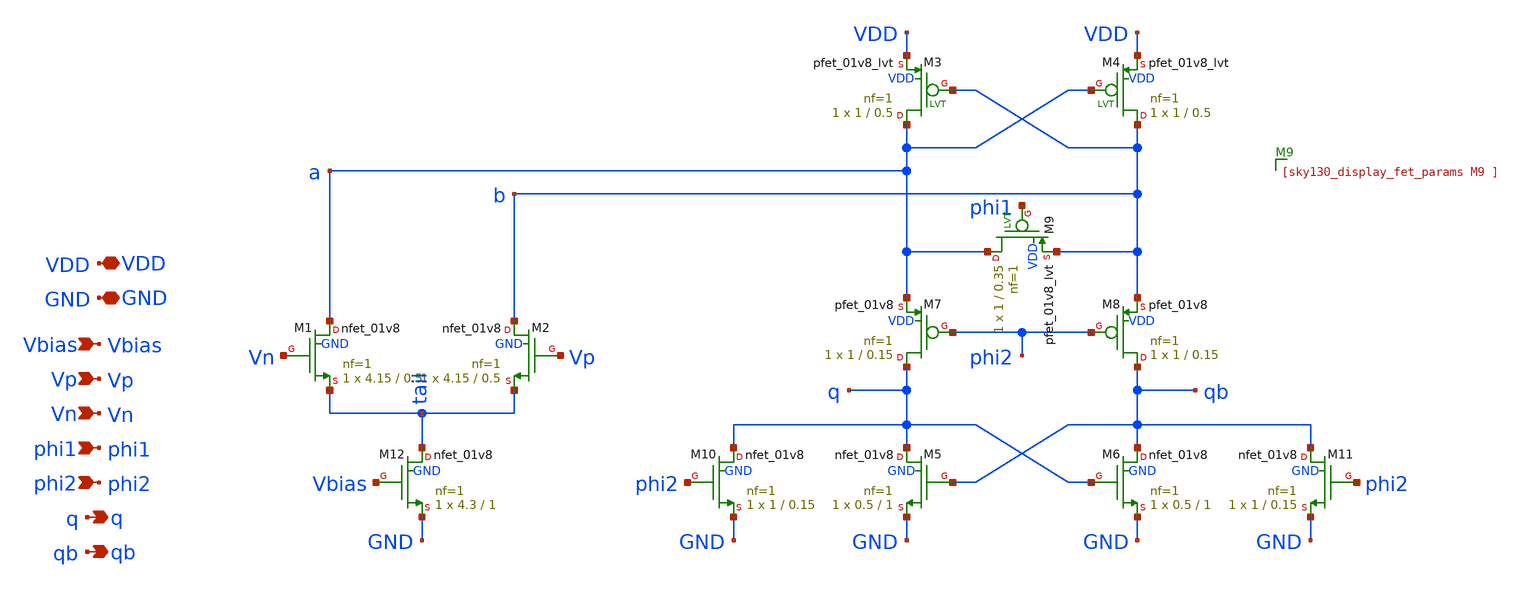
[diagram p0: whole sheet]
** sch_path: sch/comparator/comparator.sch
**.subckt comparator Vbias q VDD GND Vp Vn qb phi1 phi2
*.ipin Vbias
*.opin q
*.iopin VDD
*.iopin GND
*.ipin Vp
*.ipin Vn
*.opin qb
*.ipin phi1
*.ipin phi2
XM1 a Vn tail GND sky130_fd_pr__nfet_01v8 L=0.5 W=4.15 nf=1 ad='int((1 + 1)/2) * 4.15 / 1 * 0.29' as='int((1 + 2)/2) * 4.15 / 1 * 0.29'
+ pd='2*int((1 + 1)/2) * (4.15 / 1 + 0.29)' ps='2*int((1 + 2)/2) * (4.15 / 1 + 0.29)' nrd='0.29 / 4.15 '
+ nrs='0.29 / 4.15 ' sa=0 sb=0 sd=0 mult=1 m=1
XM2 b Vp tail GND sky130_fd_pr__nfet_01v8 L=0.5 W=4.15 nf=1 ad='int((1 + 1)/2) * 4.15 / 1 * 0.29' as='int((1 + 2)/2) * 4.15 / 1 * 0.29'
+ pd='2*int((1 + 1)/2) * (4.15 / 1 + 0.29)' ps='2*int((1 + 2)/2) * (4.15 / 1 + 0.29)' nrd='0.29 / 4.15 '
+ nrs='0.29 / 4.15 ' sa=0 sb=0 sd=0 mult=1 m=1
XM12 tail Vbias GND GND sky130_fd_pr__nfet_01v8 L=1 W=4.3 nf=1 ad='int((1 + 1)/2) * 4.3 / 1 * 0.29' as='int((1 + 2)/2) * 4.3 / 1 * 0.29'
+ pd='2*int((1 + 1)/2) * (4.3 / 1 + 0.29)' ps='2*int((1 + 2)/2) * (4.3 / 1 + 0.29)' nrd='0.29 / 4.3 ' nrs='0.29 / 4.3 '
+ sa=0 sb=0 sd=0 mult=1 m=1
XM10 q phi2 GND GND sky130_fd_pr__nfet_01v8 L=0.15 W=1 nf=1 ad='int((1 + 1)/2) * 1 / 1 * 0.29' as='int((1 + 2)/2) * 1 / 1 * 0.29'
+ pd='2*int((1 + 1)/2) * (1 / 1 + 0.29)' ps='2*int((1 + 2)/2) * (1 / 1 + 0.29)' nrd='0.29 / 1 ' nrs='0.29 / 1 '
+ sa=0 sb=0 sd=0 mult=1 m=1
XM5 q qb GND GND sky130_fd_pr__nfet_01v8 L=1 W=0.5 nf=1 ad='int((1 + 1)/2) * 0.5 / 1 * 0.29' as='int((1 + 2)/2) * 0.5 / 1 * 0.29'
+ pd='2*int((1 + 1)/2) * (0.5 / 1 + 0.29)' ps='2*int((1 + 2)/2) * (0.5 / 1 + 0.29)' nrd='0.29 / 0.5 ' nrs='0.29 / 0.5 '
+ sa=0 sb=0 sd=0 mult=1 m=1
XM6 qb q GND GND sky130_fd_pr__nfet_01v8 L=1 W=0.5 nf=1 ad='int((1 + 1)/2) * 0.5 / 1 * 0.29' as='int((1 + 2)/2) * 0.5 / 1 * 0.29'
+ pd='2*int((1 + 1)/2) * (0.5 / 1 + 0.29)' ps='2*int((1 + 2)/2) * (0.5 / 1 + 0.29)' nrd='0.29 / 0.5 ' nrs='0.29 / 0.5 '
+ sa=0 sb=0 sd=0 mult=1 m=1
XM11 qb phi2 GND GND sky130_fd_pr__nfet_01v8 L=0.15 W=1 nf=1 ad='int((1 + 1)/2) * 1 / 1 * 0.29' as='int((1 + 2)/2) * 1 / 1 * 0.29'
+ pd='2*int((1 + 1)/2) * (1 / 1 + 0.29)' ps='2*int((1 + 2)/2) * (1 / 1 + 0.29)' nrd='0.29 / 1 ' nrs='0.29 / 1 '
+ sa=0 sb=0 sd=0 mult=1 m=1
XM8 qb phi2 b VDD sky130_fd_pr__pfet_01v8 L=0.15 W=1 nf=1 ad='int((1 + 1)/2) * 1 / 1 * 0.29' as='int((1 + 2)/2) * 1 / 1 * 0.29'
+ pd='2*int((1 + 1)/2) * (1 / 1 + 0.29)' ps='2*int((1 + 2)/2) * (1 / 1 + 0.29)' nrd='0.29 / 1 ' nrs='0.29 / 1 '
+ sa=0 sb=0 sd=0 mult=1 m=1
XM7 q phi2 a VDD sky130_fd_pr__pfet_01v8 L=0.15 W=1 nf=1 ad='int((1 + 1)/2) * 1 / 1 * 0.29' as='int((1 + 2)/2) * 1 / 1 * 0.29'
+ pd='2*int((1 + 1)/2) * (1 / 1 + 0.29)' ps='2*int((1 + 2)/2) * (1 / 1 + 0.29)' nrd='0.29 / 1 ' nrs='0.29 / 1 '
+ sa=0 sb=0 sd=0 mult=1 m=1
XM3 a b VDD VDD sky130_fd_pr__pfet_01v8_lvt L=0.5 W=1 nf=1 ad='int((1 + 1)/2) * 1 / 1 * 0.29' as='int((1 + 2)/2) * 1 / 1 * 0.29'
+ pd='2*int((1 + 1)/2) * (1 / 1 + 0.29)' ps='2*int((1 + 2)/2) * (1 / 1 + 0.29)' nrd='0.29 / 1 ' nrs='0.29 / 1 '
+ sa=0 sb=0 sd=0 mult=1 m=1
XM4 b a VDD VDD sky130_fd_pr__pfet_01v8_lvt L=0.5 W=1 nf=1 ad='int((1 + 1)/2) * 1 / 1 * 0.29' as='int((1 + 2)/2) * 1 / 1 * 0.29'
+ pd='2*int((1 + 1)/2) * (1 / 1 + 0.29)' ps='2*int((1 + 2)/2) * (1 / 1 + 0.29)' nrd='0.29 / 1 ' nrs='0.29 / 1 '
+ sa=0 sb=0 sd=0 mult=1 m=1
XM9 a phi1 b VDD sky130_fd_pr__pfet_01v8_lvt L=0.35 W=1 nf=1 ad='int((1 + 1)/2) * 1 / 1 * 0.29' as='int((1 + 2)/2) * 1 / 1 * 0.29'
+ pd='2*int((1 + 1)/2) * (1 / 1 + 0.29)' ps='2*int((1 + 2)/2) * (1 / 1 + 0.29)' nrd='0.29 / 1 ' nrs='0.29 / 1 '
+ sa=0 sb=0 sd=0 mult=1 m=1
**.ends
.end
